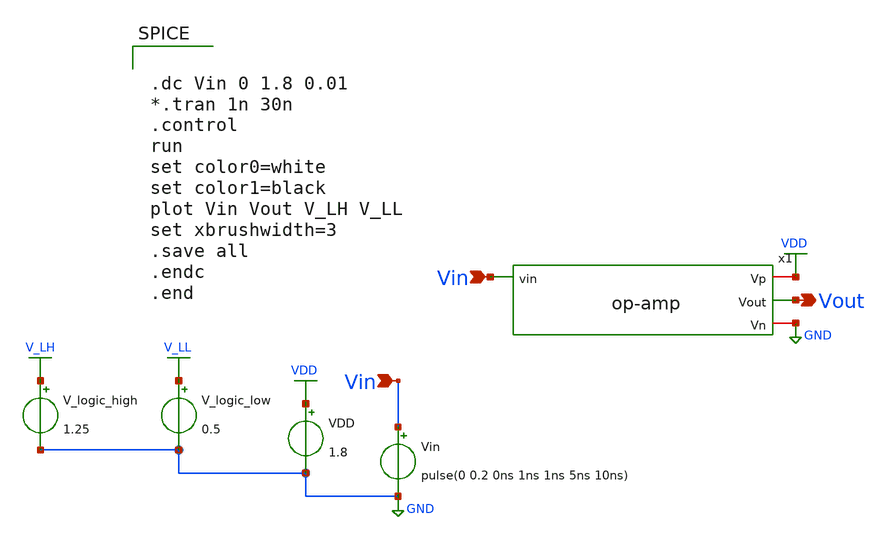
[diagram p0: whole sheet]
** sch_path: xschem/Vth_sch/Pre_layout/th01_test.sch
**.subckt th01_test Vin Vout Vin
*.ipin Vin
*.opin Vout
*.ipin Vin
VDD VDD GND 1.8
Vin Vin GND pulse(0 0.2 0ns 1ns 1ns 5ns 10ns)
V_logic_high V_LH GND 1.25
V_logic_low V_LL GND 0.5
x1 VDD Vin Vout GND op-amp
**** begin user architecture code


.lib /usr/local/share/pdk/sky130A/libs.tech/ngspice/sky130.lib.spice tt

.save all





.dc Vin 0 1.8 0.01
*.tran 1n 30n
.control
run
set color0=white
set color1=black
plot Vin Vout V_LH V_LL
set xbrushwidth=3
.save all
.endc
.end


**** end user architecture code
**.ends

* expanding   symbol:  /home/exotic/Desktop/ASIC_ADC/xschem/Vth_sch/Symbol/op-amp.sym # of pins=4
** sym_path: xschem/Vth_sch/op-amp.sym
** sch_path: xschem/Vth_sch/op-amp.sch
.subckt op-amp Vp vin Vout Vn
*.ipin vin
*.iopin Vp
*.iopin Vn
*.opin Vout
XM1 Vp vin Vout Vout sky130_fd_pr__nfet_01v8 L=4.3 W=0.42 nf=1 ad='int((nf+1)/2) * W/nf * 0.29' as='int((nf+2)/2) * W/nf * 0.29'
+ pd='2*int((nf+1)/2) * (W/nf + 0.29)' ps='2*int((nf+2)/2) * (W/nf + 0.29)' nrd='0.29 / W' nrs='0.29 / W'
+ sa=0 sb=0 sd=0 mult=1 m=1
XM2 Vn vin Vout Vout sky130_fd_pr__pfet_01v8 L=0.25 W=1.5 nf=1 ad='int((nf+1)/2) * W/nf * 0.29' as='int((nf+2)/2) * W/nf * 0.29'
+ pd='2*int((nf+1)/2) * (W/nf + 0.29)' ps='2*int((nf+2)/2) * (W/nf + 0.29)' nrd='0.29 / W' nrs='0.29 / W'
+ sa=0 sb=0 sd=0 mult=1 m=1
.ends

.GLOBAL VDD
.GLOBAL GND
.GLOBAL V_LH
.GLOBAL V_LL
.end
